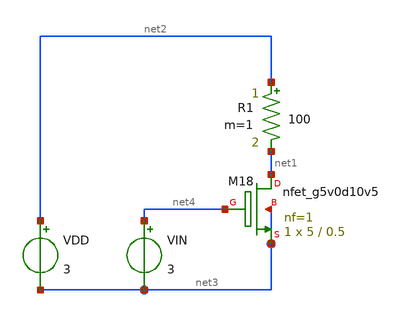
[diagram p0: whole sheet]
** sch_path: xschem/untitled.sch
**.subckt untitled
XM18 net1 net4 net3 net3 sky130_fd_pr__nfet_g5v0d10v5 L=0.5 W=5 nf=1 ad='int((nf+1)/2) * W/nf * 0.29'
+ as='int((nf+2)/2) * W/nf * 0.29' pd='2*int((nf+1)/2) * (W/nf + 0.29)' ps='2*int((nf+2)/2) * (W/nf + 0.29)'
+ nrd='0.29 / W' nrs='0.29 / W' sa=0 sb=0 sd=0 mult=1 m=1
VIN net4 net3 3
VDD net2 net3 3
R1 net2 net1 100 m=1
**** begin user architecture code


.lib /usr/local/share/pdk/sky130A/libs.tech/ngspice/sky130.lib.spice tt
.include /usr/local/share/pdk/sky130A/libs.ref/sky130_fd_sc_hvl/spice/sky130_fd_sc_hvl.spice




.DC VDD 0 7 0.1 VIN 0 5 1
.CONTROL
RUN
PLOT -VDD#BRANCH
.ENDC

**** end user architecture code
**.ends
.end
